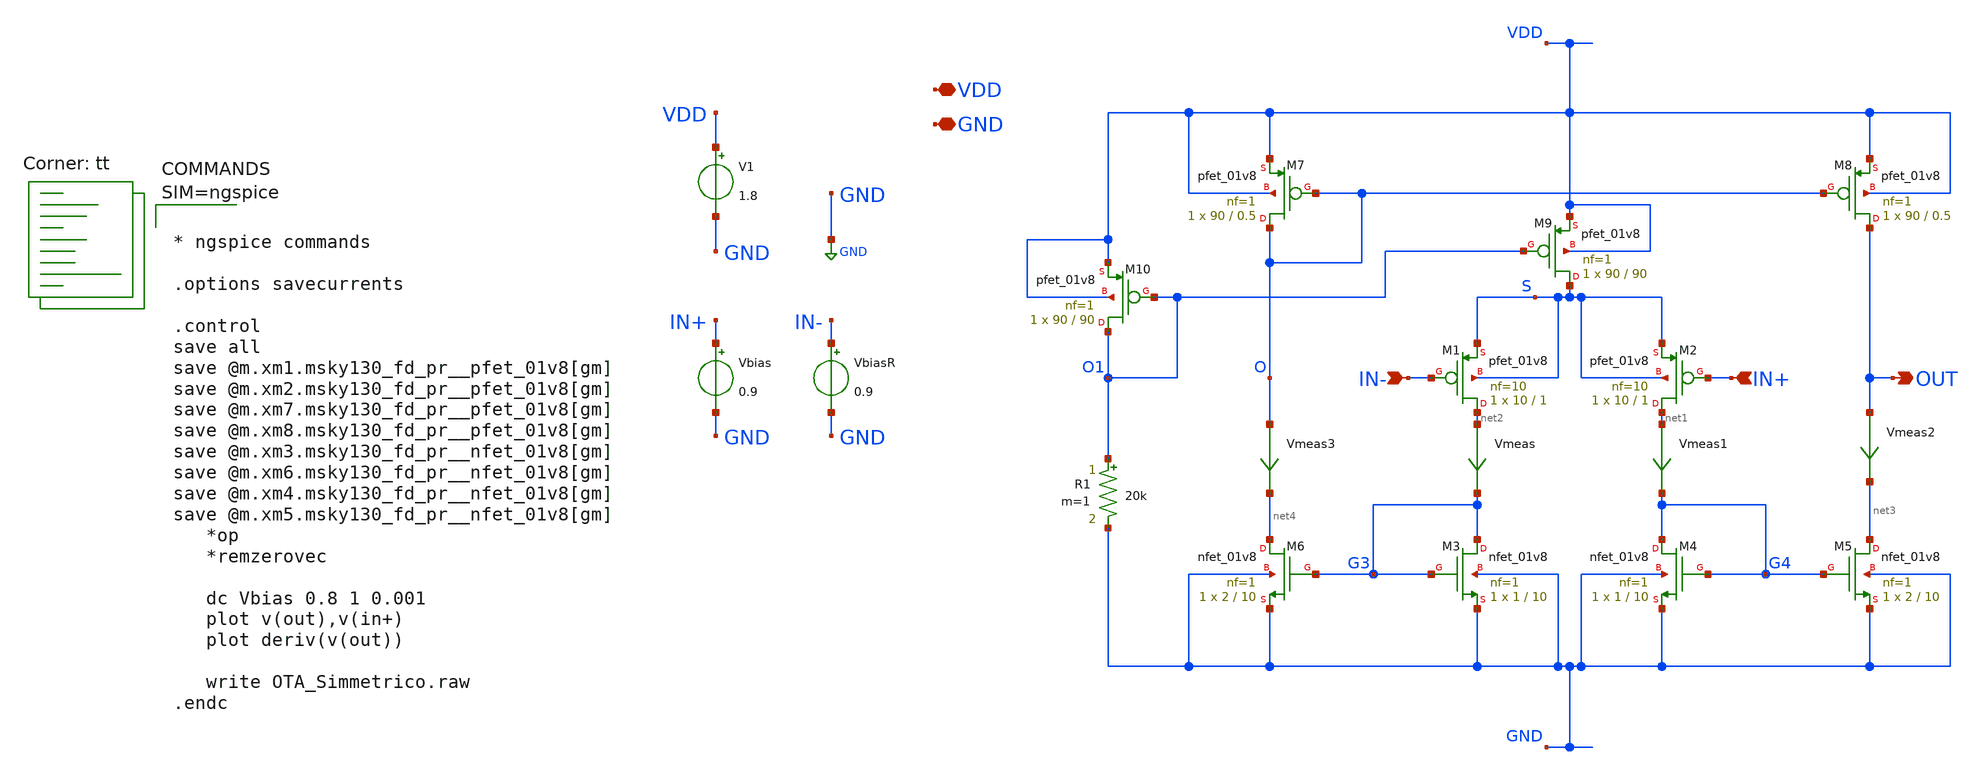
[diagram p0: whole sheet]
** sch_path: xschem/OTA_Simmetrico.sch
**.subckt OTA_Simmetrico VDD GND IN+ IN- OUT
*.iopin VDD
*.iopin GND
*.ipin IN+
*.ipin IN-
*.opin OUT
XM1 net2 IN- S S sky130_fd_pr__pfet_01v8 L=1 W=10 nf=10 ad='int((nf+1)/2) * W/nf * 0.29' as='int((nf+2)/2) * W/nf * 0.29'
+ pd='2*int((nf+1)/2) * (W/nf + 0.29)' ps='2*int((nf+2)/2) * (W/nf + 0.29)' nrd='0.29 / W' nrs='0.29 / W'
+ sa=0 sb=0 sd=0 mult=1 m=1
XM2 net1 IN+ S S sky130_fd_pr__pfet_01v8 L=1 W=10 nf=10 ad='int((nf+1)/2) * W/nf * 0.29' as='int((nf+2)/2) * W/nf * 0.29'
+ pd='2*int((nf+1)/2) * (W/nf + 0.29)' ps='2*int((nf+2)/2) * (W/nf + 0.29)' nrd='0.29 / W' nrs='0.29 / W'
+ sa=0 sb=0 sd=0 mult=1 m=1
XM3 G3 G3 GND GND sky130_fd_pr__nfet_01v8 L=10 W=1 nf=1 ad='int((nf+1)/2) * W/nf * 0.29' as='int((nf+2)/2) * W/nf * 0.29'
+ pd='2*int((nf+1)/2) * (W/nf + 0.29)' ps='2*int((nf+2)/2) * (W/nf + 0.29)' nrd='0.29 / W' nrs='0.29 / W'
+ sa=0 sb=0 sd=0 mult=1 m=1
XM4 G4 G4 GND GND sky130_fd_pr__nfet_01v8 L=10 W=1 nf=1 ad='int((nf+1)/2) * W/nf * 0.29' as='int((nf+2)/2) * W/nf * 0.29'
+ pd='2*int((nf+1)/2) * (W/nf + 0.29)' ps='2*int((nf+2)/2) * (W/nf + 0.29)' nrd='0.29 / W' nrs='0.29 / W'
+ sa=0 sb=0 sd=0 mult=1 m=1
XM5 net3 G4 GND GND sky130_fd_pr__nfet_01v8 L=10 W=2 nf=1 ad='int((nf+1)/2) * W/nf * 0.29' as='int((nf+2)/2) * W/nf * 0.29'
+ pd='2*int((nf+1)/2) * (W/nf + 0.29)' ps='2*int((nf+2)/2) * (W/nf + 0.29)' nrd='0.29 / W' nrs='0.29 / W'
+ sa=0 sb=0 sd=0 mult=1 m=1
XM6 net4 G3 GND GND sky130_fd_pr__nfet_01v8 L=10 W=2 nf=1 ad='int((nf+1)/2) * W/nf * 0.29' as='int((nf+2)/2) * W/nf * 0.29'
+ pd='2*int((nf+1)/2) * (W/nf + 0.29)' ps='2*int((nf+2)/2) * (W/nf + 0.29)' nrd='0.29 / W' nrs='0.29 / W'
+ sa=0 sb=0 sd=0 mult=1 m=1
XM7 O O VDD VDD sky130_fd_pr__pfet_01v8 L=0.5 W=90 nf=1 ad='int((nf+1)/2) * W/nf * 0.29' as='int((nf+2)/2) * W/nf * 0.29'
+ pd='2*int((nf+1)/2) * (W/nf + 0.29)' ps='2*int((nf+2)/2) * (W/nf + 0.29)' nrd='0.29 / W' nrs='0.29 / W'
+ sa=0 sb=0 sd=0 mult=1 m=1
XM8 OUT O VDD VDD sky130_fd_pr__pfet_01v8 L=0.5 W=90 nf=1 ad='int((nf+1)/2) * W/nf * 0.29' as='int((nf+2)/2) * W/nf * 0.29'
+ pd='2*int((nf+1)/2) * (W/nf + 0.29)' ps='2*int((nf+2)/2) * (W/nf + 0.29)' nrd='0.29 / W' nrs='0.29 / W'
+ sa=0 sb=0 sd=0 mult=1 m=1
V1 VDD GND 1.8
Vbias IN+ GND 0.9
VbiasR IN- GND 0.9
Vmeas net2 G3 0
.save i(vmeas)
Vmeas1 net1 G4 0
.save i(vmeas1)
Vmeas2 OUT net3 0
.save i(vmeas2)
Vmeas3 O net4 0
.save i(vmeas3)
XM9 S O1 VDD VDD sky130_fd_pr__pfet_01v8 L=90 W=90 nf=1 ad='int((nf+1)/2) * W/nf * 0.29' as='int((nf+2)/2) * W/nf * 0.29'
+ pd='2*int((nf+1)/2) * (W/nf + 0.29)' ps='2*int((nf+2)/2) * (W/nf + 0.29)' nrd='0.29 / W' nrs='0.29 / W'
+ sa=0 sb=0 sd=0 mult=1 m=1
XM10 O1 O1 VDD VDD sky130_fd_pr__pfet_01v8 L=90 W=90 nf=1 ad='int((nf+1)/2) * W/nf * 0.29' as='int((nf+2)/2) * W/nf * 0.29'
+ pd='2*int((nf+1)/2) * (W/nf + 0.29)' ps='2*int((nf+2)/2) * (W/nf + 0.29)' nrd='0.29 / W' nrs='0.29 / W'
+ sa=0 sb=0 sd=0 mult=1 m=1
R1 O1 GND 20k m=1
**** begin user architecture code



* ngspice commands

.options savecurrents

.control
save all
save @m.xm1.msky130_fd_pr__pfet_01v8[gm]
save @m.xm2.msky130_fd_pr__pfet_01v8[gm]
save @m.xm7.msky130_fd_pr__pfet_01v8[gm]
save @m.xm8.msky130_fd_pr__pfet_01v8[gm]
save @m.xm3.msky130_fd_pr__nfet_01v8[gm]
save @m.xm6.msky130_fd_pr__nfet_01v8[gm]
save @m.xm4.msky130_fd_pr__nfet_01v8[gm]
save @m.xm5.msky130_fd_pr__nfet_01v8[gm]
   *op
   *remzerovec

   dc Vbias 0.8 1 0.001
   plot v(out),v(in+)
   plot deriv(v(out))

   write OTA_Simmetrico.raw
.endc




.lib $::SKYWATER_MODELS/sky130.lib.spice tt
**** end user architecture code
**.ends
.GLOBAL GND
.end
